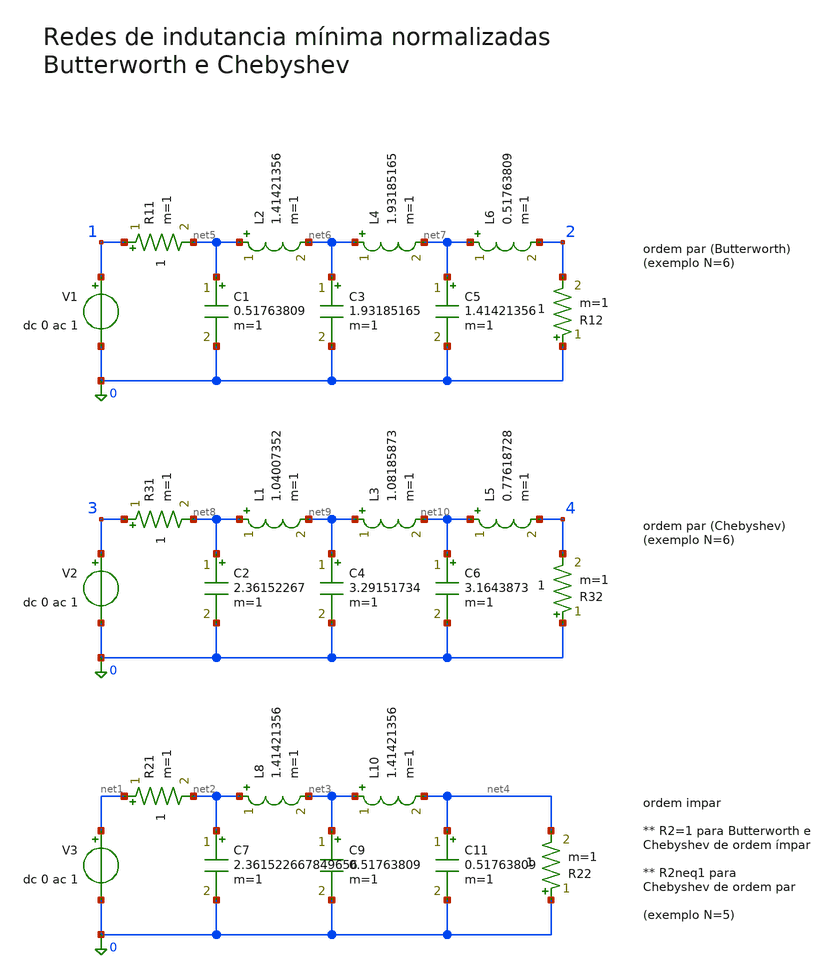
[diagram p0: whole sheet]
** sch_path: circuitos/exemplo08.sch
**.subckt exemplo08
V1 1 0 dc 0 ac 1
R21 net1 net2 1 m=1
R22 0 net4 1 m=1
C1 net5 0 0.51763809 m=1
V2 3 0 dc 0 ac 1
R11 1 net5 1 m=1
C3 net6 0 1.93185165 m=1
C5 net7 0 1.41421356 m=1
R12 0 2 1 m=1
L2 net5 net6 1.41421356 m=1
L4 net6 net7 1.93185165 m=1
L6 net7 2 0.51763809 m=1
C7 net2 0 2.361522667849656 m=1
L8 net2 net3 1.41421356 m=1
C9 net3 0 0.51763809 m=1
L10 net3 net4 1.41421356 m=1
C11 net4 0 0.51763809 m=1
V3 net1 0 dc 0 ac 1
C2 net8 0 2.36152267 m=1
R31 3 net8 1 m=1
C4 net9 0 3.29151734 m=1
C6 net10 0 3.1643873 m=1
R32 0 4 1 m=1
L1 net8 net9 1.04007352 m=1
L3 net9 net10 1.08185873 m=1
L5 net10 4 0.77618728 m=1
**** begin user architecture code

.control

ac dec 100 0.016 1.59
let w = 2*PI*frequency
plot xlog db(-v(2)/v(1)) vs w
plot xlog db(-v(4)/v(3)) vs w

*ac dec 100 1e-1 1e1
*plot xlog db(-v(2)/v(1))
*plot xlog db(-v(4)/v(3))

.endc

**** end user architecture code
**.ends
.end
